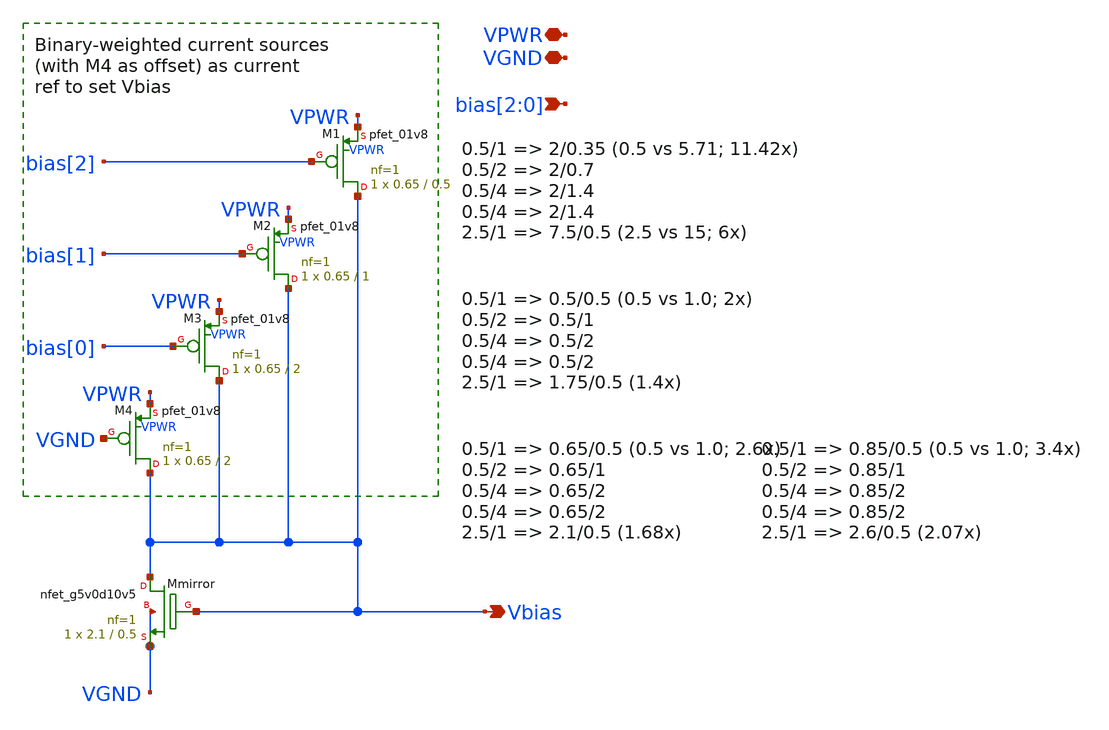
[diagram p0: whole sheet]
** sch_path: xschem-cascode-backup/vbias2p5x.sch
**.subckt vbias2p5x VPWR VGND bias[2],bias[1],bias[0] Vbias
*.iopin VPWR
*.iopin VGND
*.ipin bias[2],bias[1],bias[0]
*.opin Vbias
XM1 Vbias bias[2] VPWR VPWR sky130_fd_pr__pfet_01v8 L=0.5 W=0.65 nf=1 ad='int((nf+1)/2) * W/nf * 0.29'
+ as='int((nf+2)/2) * W/nf * 0.29' pd='2*int((nf+1)/2) * (W/nf + 0.29)' ps='2*int((nf+2)/2) * (W/nf + 0.29)'
+ nrd='0.29 / W' nrs='0.29 / W' sa=0 sb=0 sd=0 mult=1 m=1
XM2 Vbias bias[1] VPWR VPWR sky130_fd_pr__pfet_01v8 L=1 W=0.65 nf=1 ad='int((nf+1)/2) * W/nf * 0.29'
+ as='int((nf+2)/2) * W/nf * 0.29' pd='2*int((nf+1)/2) * (W/nf + 0.29)' ps='2*int((nf+2)/2) * (W/nf + 0.29)'
+ nrd='0.29 / W' nrs='0.29 / W' sa=0 sb=0 sd=0 mult=1 m=1
XM3 Vbias bias[0] VPWR VPWR sky130_fd_pr__pfet_01v8 L=2 W=0.65 nf=1 ad='int((nf+1)/2) * W/nf * 0.29'
+ as='int((nf+2)/2) * W/nf * 0.29' pd='2*int((nf+1)/2) * (W/nf + 0.29)' ps='2*int((nf+2)/2) * (W/nf + 0.29)'
+ nrd='0.29 / W' nrs='0.29 / W' sa=0 sb=0 sd=0 mult=1 m=1
XMmirror Vbias Vbias VGND VGND sky130_fd_pr__nfet_g5v0d10v5 L=0.5 W=2.1 nf=1 ad='int((nf+1)/2) * W/nf * 0.29'
+ as='int((nf+2)/2) * W/nf * 0.29' pd='2*int((nf+1)/2) * (W/nf + 0.29)' ps='2*int((nf+2)/2) * (W/nf + 0.29)'
+ nrd='0.29 / W' nrs='0.29 / W' sa=0 sb=0 sd=0 mult=1 m=1
XM4 Vbias VGND VPWR VPWR sky130_fd_pr__pfet_01v8 L=2 W=0.65 nf=1 ad='int((nf+1)/2) * W/nf * 0.29' as='int((nf+2)/2) * W/nf * 0.29'
+ pd='2*int((nf+1)/2) * (W/nf + 0.29)' ps='2*int((nf+2)/2) * (W/nf + 0.29)' nrd='0.29 / W' nrs='0.29 / W'
+ sa=0 sb=0 sd=0 mult=1 m=1
**.ends
.end
